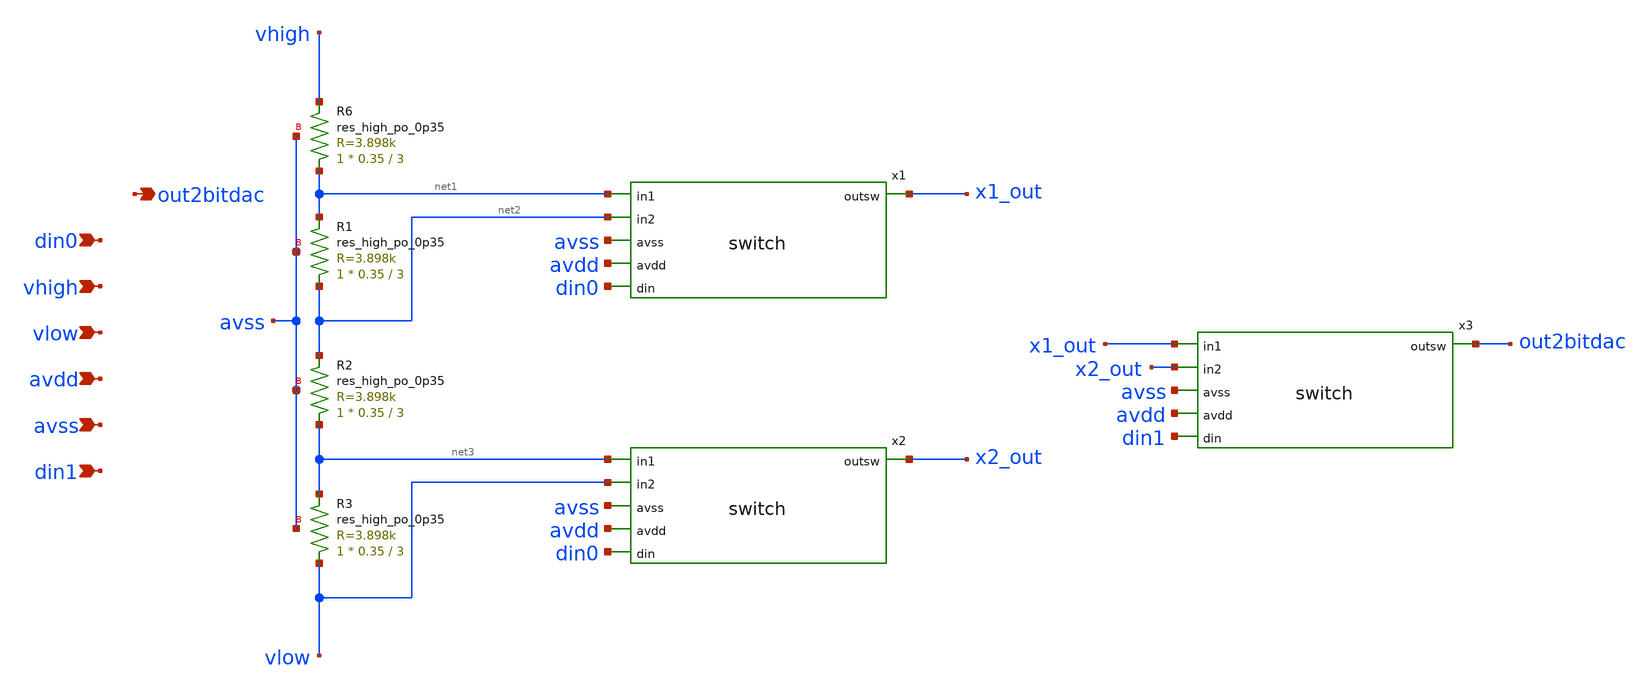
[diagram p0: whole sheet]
** sch_path: xschem/2bitdac.sch
**.subckt 2bitdac din0 vhigh vlow avdd avss din1 out2bitdac
*.ipin din0
*.ipin vhigh
*.ipin vlow
*.ipin avdd
*.ipin avss
*.ipin din1
*.opin out2bitdac
x1 x1_out net1 net2 avss avdd din0 switch
x2 x2_out net3 vlow avss avdd din0 switch
x3 out2bitdac x1_out x2_out avss avdd din1 switch
XR6 net1 vhigh avss sky130_fd_pr__res_high_po_0p35 L=3 mult=1 m=1
XR1 net2 net1 avss sky130_fd_pr__res_high_po_0p35 L=3 mult=1 m=1
XR2 net3 net2 avss sky130_fd_pr__res_high_po_0p35 L=3 mult=1 m=1
XR3 vlow net3 avss sky130_fd_pr__res_high_po_0p35 L=3 mult=1 m=1
**.ends

* expanding   symbol:  switch.sym # of pins=6
** sym_path: xschem/switch.sym
** sch_path: xschem/switch.sch
.subckt switch outsw in1 in2 avss avdd din
*.ipin avss
*.ipin avdd
*.ipin din
*.ipin in1
*.ipin in2
*.opin outsw
XM10 dinbar din avdd avdd sky130_fd_pr__pfet_g5v0d10v5 L=0.5 W=1 nf=1 ad='int((1 + 1)/2) * 1 / 1 * 0.29'
+ as='int((1 + 2)/2) * 1 / 1 * 0.29' pd='2*int((1 + 1)/2) * (1 / 1 + 0.29)' ps='2*int((1 + 2)/2) * (1 / 1 + 0.29)'
+ nrd='0.29 / 1 ' nrs='0.29 / 1 ' sa=0 sb=0 sd=0 mult=1 m=1
XM2 dinbar din avss avss sky130_fd_pr__nfet_g5v0d10v5 L=0.5 W=1 nf=1 ad='int((1 + 1)/2) * 1 / 1 * 0.29'
+ as='int((1 + 2)/2) * 1 / 1 * 0.29' pd='2*int((1 + 1)/2) * (1 / 1 + 0.29)' ps='2*int((1 + 2)/2) * (1 / 1 + 0.29)'
+ nrd='0.29 / 1 ' nrs='0.29 / 1 ' sa=0 sb=0 sd=0 mult=1 m=1
XM1 wc dinbar avdd avdd sky130_fd_pr__pfet_g5v0d10v5 L=0.5 W=1 nf=1 ad='int((1 + 1)/2) * 1 / 1 * 0.29'
+ as='int((1 + 2)/2) * 1 / 1 * 0.29' pd='2*int((1 + 1)/2) * (1 / 1 + 0.29)' ps='2*int((1 + 2)/2) * (1 / 1 + 0.29)'
+ nrd='0.29 / 1 ' nrs='0.29 / 1 ' sa=0 sb=0 sd=0 mult=1 m=1
XM3 wc dinbar avss avss sky130_fd_pr__nfet_g5v0d10v5 L=0.5 W=1 nf=1 ad='int((1 + 1)/2) * 1 / 1 * 0.29'
+ as='int((1 + 2)/2) * 1 / 1 * 0.29' pd='2*int((1 + 1)/2) * (1 / 1 + 0.29)' ps='2*int((1 + 2)/2) * (1 / 1 + 0.29)'
+ nrd='0.29 / 1 ' nrs='0.29 / 1 ' sa=0 sb=0 sd=0 mult=1 m=1
XM5 outsw dinbar in2 avss sky130_fd_pr__nfet_g5v0d10v5 L=0.5 W=1 nf=1 ad='int((1 + 1)/2) * 1 / 1 * 0.29'
+ as='int((1 + 2)/2) * 1 / 1 * 0.29' pd='2*int((1 + 1)/2) * (1 / 1 + 0.29)' ps='2*int((1 + 2)/2) * (1 / 1 + 0.29)'
+ nrd='0.29 / 1 ' nrs='0.29 / 1 ' sa=0 sb=0 sd=0 mult=1 m=1
XM4 outsw dinbar in1 avdd sky130_fd_pr__pfet_g5v0d10v5 L=0.5 W=1 nf=1 ad='int((1 + 1)/2) * 1 / 1 * 0.29'
+ as='int((1 + 2)/2) * 1 / 1 * 0.29' pd='2*int((1 + 1)/2) * (1 / 1 + 0.29)' ps='2*int((1 + 2)/2) * (1 / 1 + 0.29)'
+ nrd='0.29 / 1 ' nrs='0.29 / 1 ' sa=0 sb=0 sd=0 mult=1 m=1
XM11 in2 wc outsw avdd sky130_fd_pr__pfet_g5v0d10v5 L=0.5 W=1 nf=1 ad='int((1 + 1)/2) * 1 / 1 * 0.29'
+ as='int((1 + 2)/2) * 1 / 1 * 0.29' pd='2*int((1 + 1)/2) * (1 / 1 + 0.29)' ps='2*int((1 + 2)/2) * (1 / 1 + 0.29)'
+ nrd='0.29 / 1 ' nrs='0.29 / 1 ' sa=0 sb=0 sd=0 mult=1 m=1
XM12 in1 wc outsw avss sky130_fd_pr__nfet_g5v0d10v5 L=0.5 W=1 nf=1 ad='int((1 + 1)/2) * 1 / 1 * 0.29'
+ as='int((1 + 2)/2) * 1 / 1 * 0.29' pd='2*int((1 + 1)/2) * (1 / 1 + 0.29)' ps='2*int((1 + 2)/2) * (1 / 1 + 0.29)'
+ nrd='0.29 / 1 ' nrs='0.29 / 1 ' sa=0 sb=0 sd=0 mult=1 m=1
.ends

.end
